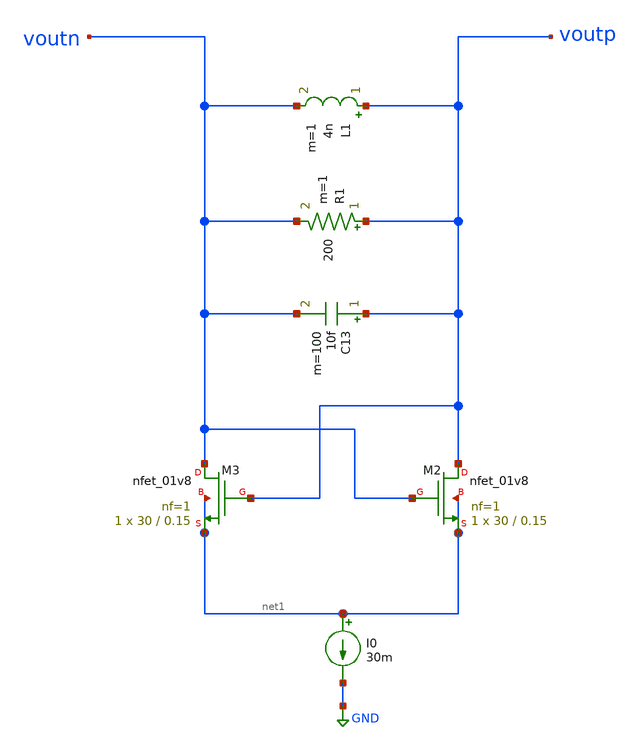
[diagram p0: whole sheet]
** sch_path: pll/lc_vco_lib/Ahmed_Reda/VCO_NMOS_init/xschem/VCO_NMOS_init.sch
**.subckt VCO_NMOS_init
XM2 voutp voutn net1 net1 sky130_fd_pr__nfet_01v8 L=0.15 W=30 nf=1 ad='int((1 + 1)/2) * 30 / 1 * 0.29'
+ as='int((1 + 2)/2) * 30 / 1 * 0.29' pd='2*int((1 + 1)/2) * (30 / 1 + 0.29)' ps='2*int((1 + 2)/2) * (30 / 1 + 0.29)'
+ nrd='0.29 / 30 ' nrs='0.29 / 30 ' sa=0 sb=0 sd=0 mult=1 m=1
XM3 voutn voutp net1 net1 sky130_fd_pr__nfet_01v8 L=0.15 W=30 nf=1 ad='int((1 + 1)/2) * 30 / 1 * 0.29'
+ as='int((1 + 2)/2) * 30 / 1 * 0.29' pd='2*int((1 + 1)/2) * (30 / 1 + 0.29)' ps='2*int((1 + 2)/2) * (30 / 1 + 0.29)'
+ nrd='0.29 / 30 ' nrs='0.29 / 30 ' sa=0 sb=0 sd=0 mult=1 m=1
L1 voutp voutn 4n m=1
I0 net1 GND 30m
C13 voutp voutn 10f m=100
R1 voutp voutn 200 m=1
**.ends
.GLOBAL GND
.end
